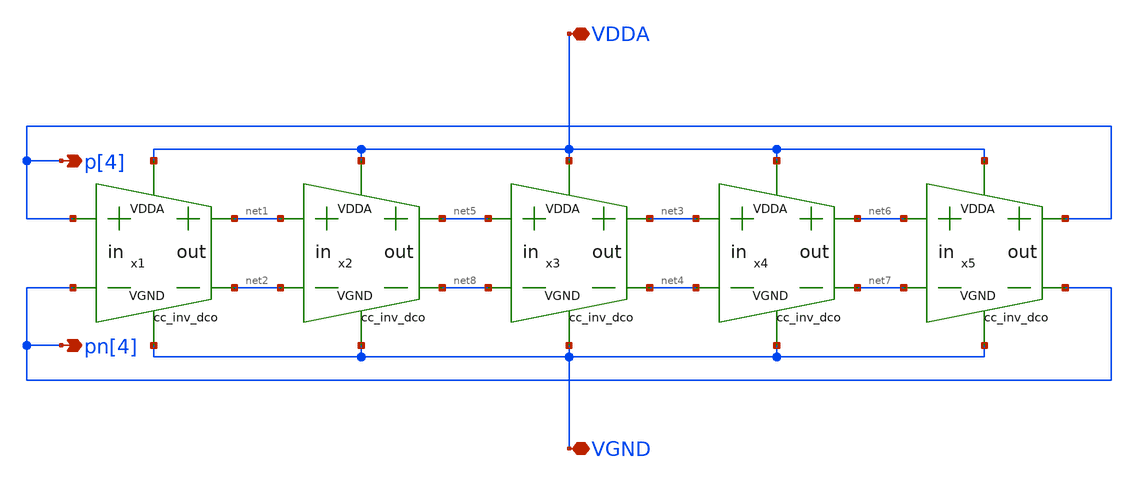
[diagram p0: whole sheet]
** sch_path: xschem/lib/x5s_cc_osc_dco.sch
**.subckt x5s_cc_osc_dco VDDA VGND p[4] pn[4]
*.iopin VDDA
*.iopin VGND
*.opin p[4]
*.opin pn[4]
x1 VDDA net1 p[4] pn[4] net2 VGND cc_inv_dco
x2 VDDA net5 net1 net2 net8 VGND cc_inv_dco
x3 VDDA net3 net5 net8 net4 VGND cc_inv_dco
x4 VDDA net6 net3 net4 net7 VGND cc_inv_dco
x5 VDDA p[4] net6 net7 pn[4] VGND cc_inv_dco
**.ends

* expanding   symbol:  ../lib/cc_inv_dco.sym # of pins=6
** sym_path: xschem/lib/cc_inv_dco.sym
** sch_path: xschem/lib/cc_inv_dco.sch
.subckt cc_inv_dco VDDA outp inp inn outn VGND
*.opin outp
*.ipin inn
*.iopin VGND
*.opin outn
*.ipin inp
*.iopin VDDA
x1 VDDA VGND outp inp main_inv_dco
x2 VPWR VGND outn inn main_inv_dco
x3 outp outn VDDA VGND aux_inv_dco
x4 outn outp VDDA VGND aux_inv_dco
.ends


* expanding   symbol:  ../lib/main_inv_dco.sym # of pins=4
** sym_path: xschem/lib/main_inv_dco.sym
** sch_path: xschem/lib/main_inv_dco.sch
.subckt main_inv_dco VDDA VGND Y A
*.iopin VDDA
*.iopin VGND
*.ipin A
*.opin Y
XM3 Y A VGND VGND sky130_fd_pr__nfet_01v8 L=1.2 W=4 nf=2 ad='int((nf+1)/2) * W/nf * 0.29' as='int((nf+2)/2) * W/nf * 0.29'
+ pd='2*int((nf+1)/2) * (W/nf + 0.29)' ps='2*int((nf+2)/2) * (W/nf + 0.29)' nrd='0.29 / W' nrs='0.29 / W'
+ sa=0 sb=0 sd=0 mult=1 m=1
XM2 Y A VDDA VDDA sky130_fd_pr__pfet_01v8 L=1.2 W=6 nf=2 ad='int((nf+1)/2) * W/nf * 0.29' as='int((nf+2)/2) * W/nf * 0.29'
+ pd='2*int((nf+1)/2) * (W/nf + 0.29)' ps='2*int((nf+2)/2) * (W/nf + 0.29)' nrd='0.29 / W' nrs='0.29 / W'
+ sa=0 sb=0 sd=0 mult=1 m=1
.ends


* expanding   symbol:  ../lib/aux_inv_dco.sym # of pins=4
** sym_path: xschem/lib/aux_inv_dco.sym
** sch_path: xschem/lib/aux_inv_dco.sch
.subckt aux_inv_dco A Y VDDA VGND
*.iopin VDDA
*.iopin VGND
*.ipin A
*.opin Y
XM3 Y A VGND VGND sky130_fd_pr__nfet_01v8 L=1.2 W=2 nf=1 ad='int((nf+1)/2) * W/nf * 0.29' as='int((nf+2)/2) * W/nf * 0.29'
+ pd='2*int((nf+1)/2) * (W/nf + 0.29)' ps='2*int((nf+2)/2) * (W/nf + 0.29)' nrd='0.29 / W' nrs='0.29 / W'
+ sa=0 sb=0 sd=0 mult=1 m=1
XM2 Y A VDDA VDDA sky130_fd_pr__pfet_01v8 L=1.2 W=3 nf=1 ad='int((nf+1)/2) * W/nf * 0.29' as='int((nf+2)/2) * W/nf * 0.29'
+ pd='2*int((nf+1)/2) * (W/nf + 0.29)' ps='2*int((nf+2)/2) * (W/nf + 0.29)' nrd='0.29 / W' nrs='0.29 / W'
+ sa=0 sb=0 sd=0 mult=1 m=1
.ends

.end
